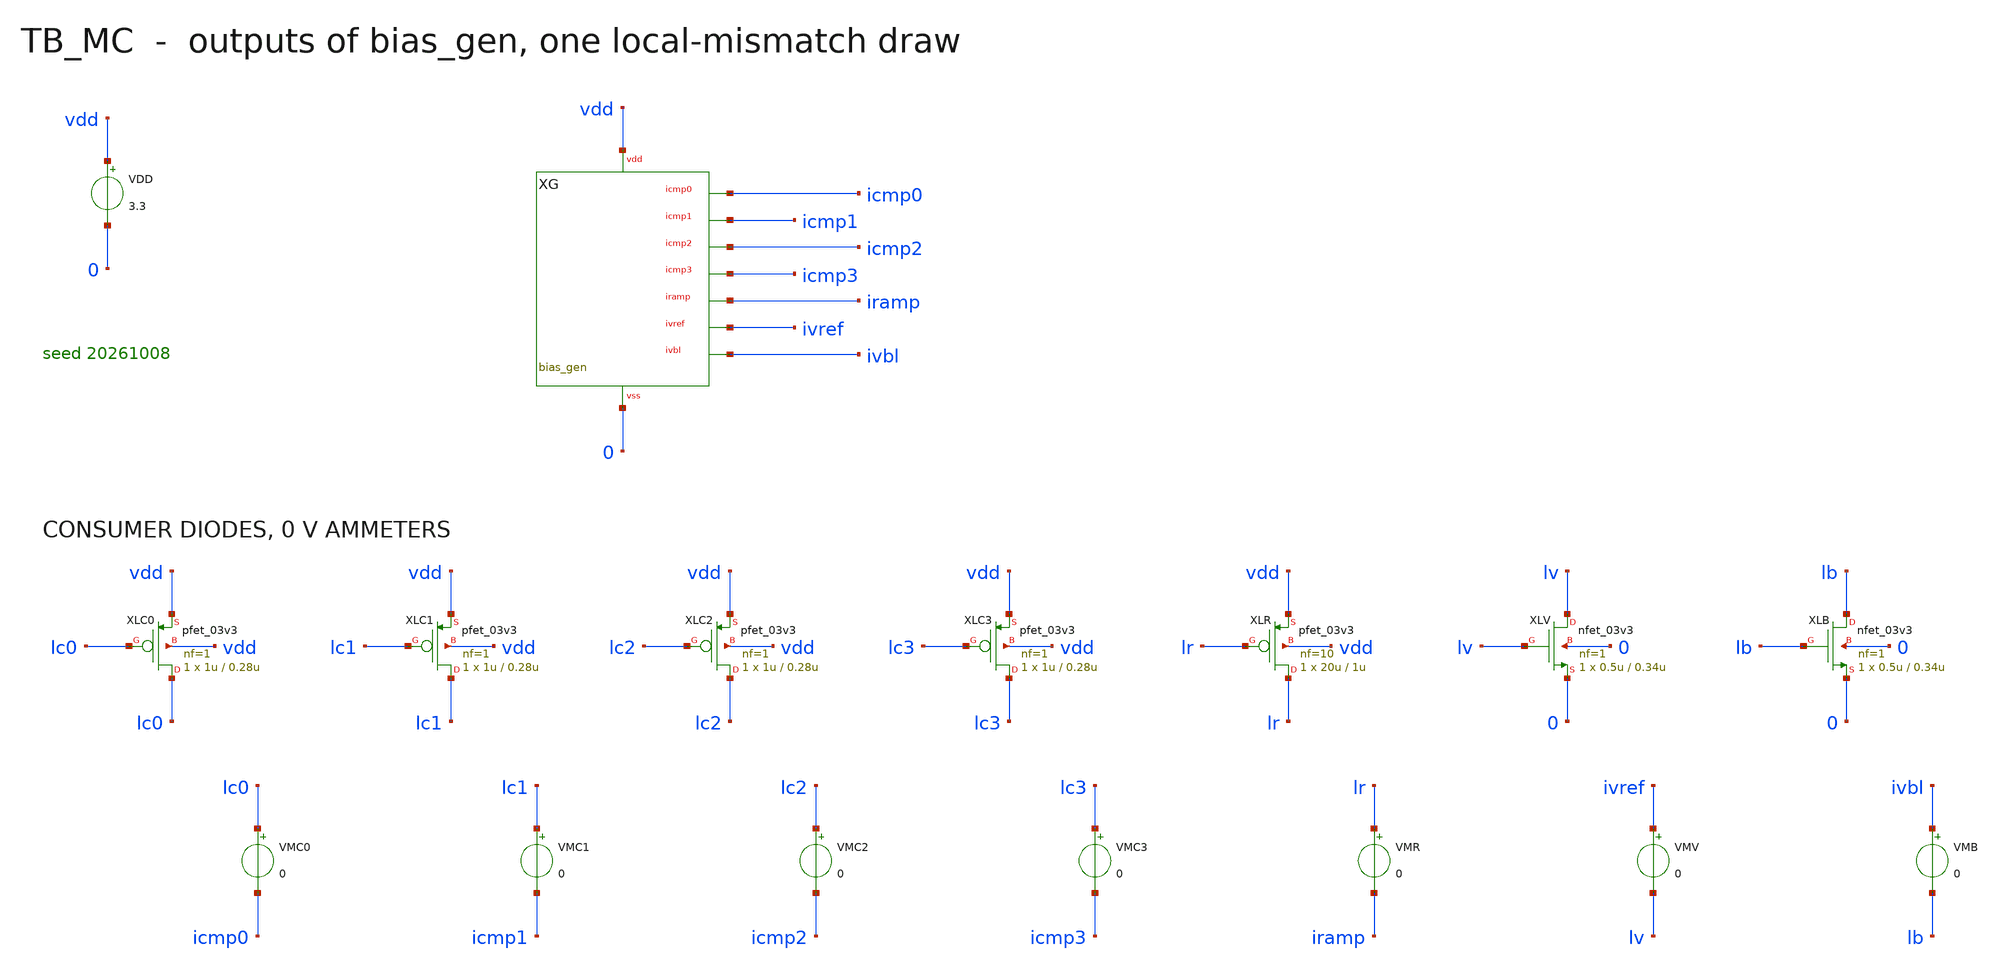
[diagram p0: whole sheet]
** sch_path: mixed_signal/bias_gen/tb_mc.sch
**.subckt tb_mc
VDD vdd 0 3.3
XG vdd 0 icmp0 icmp1 icmp2 icmp3 iramp ivref ivbl bias_gen
XLC0 lc0 lc0 vdd vdd pfet_03v3 L=0.28u W=1u nf=1 m=1 ad=0.18p pd=2.36u as=0.18p ps=2.36u nrd=0.18
+ nrs=0.18
VMC0 lc0 icmp0 0
XLC1 lc1 lc1 vdd vdd pfet_03v3 L=0.28u W=1u nf=1 m=1 ad=0.18p pd=2.36u as=0.18p ps=2.36u nrd=0.18
+ nrs=0.18
VMC1 lc1 icmp1 0
XLC2 lc2 lc2 vdd vdd pfet_03v3 L=0.28u W=1u nf=1 m=1 ad=0.18p pd=2.36u as=0.18p ps=2.36u nrd=0.18
+ nrs=0.18
VMC2 lc2 icmp2 0
XLC3 lc3 lc3 vdd vdd pfet_03v3 L=0.28u W=1u nf=1 m=1 ad=0.18p pd=2.36u as=0.18p ps=2.36u nrd=0.18
+ nrs=0.18
VMC3 lc3 icmp3 0
XLR lr lr vdd vdd pfet_03v3 L=1u W=20u nf=10 m=1 ad=1.8p pd=21.8u as=2.16p ps=26.16u nrd=0.009
+ nrs=0.009
VMR lr iramp 0
XLV lv lv 0 0 nfet_03v3 L=0.34u W=0.5u nf=1 m=1 ad=0.09p pd=1.36u as=0.09p ps=1.36u nrd=0.36
+ nrs=0.36
VMV ivref lv 0
XLB lb lb 0 0 nfet_03v3 L=0.34u W=0.5u nf=1 m=1 ad=0.09p pd=1.36u as=0.09p ps=1.36u nrd=0.36
+ nrs=0.36
VMB ivbl lb 0
**** begin user architecture code

.include /foss/pdks/gf180mcuD/libs.tech/ngspice/design.ngspice
.lib /foss/pdks/gf180mcuD/libs.tech/ngspice/sm141064.ngspice typical
.lib /foss/pdks/gf180mcuD/libs.tech/ngspice/sm141064.ngspice res_typical
.lib /foss/pdks/gf180mcuD/libs.tech/ngspice/sm141064.ngspice mimcap_typical
.param sw_stat_mismatch=1
.temp 27
.options seed=20261008
.control
set num_threads=1
op
let a0 = i(vmc0)
let a1 = i(vmc1)
let a2 = i(vmc2)
let a3 = i(vmc3)
let a4 = i(vmr)
let a5 = i(vmv)
let a6 = i(vmb)
let a7 = @m.xg.xmn1.m0[id]
echo MC 1 $&a0 $&a1 $&a2 $&a3 $&a4 $&a5 $&a6 $&a7
quit
.endc

**** end user architecture code
**.ends
.end
